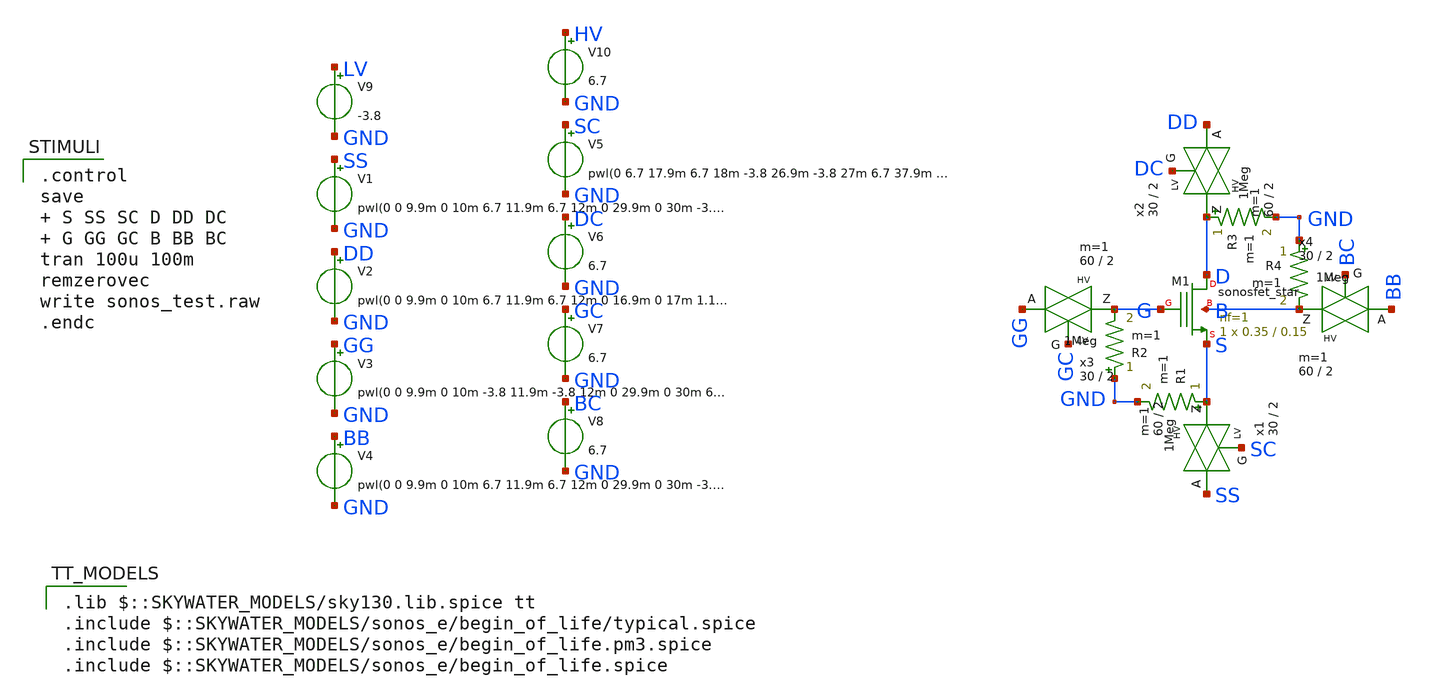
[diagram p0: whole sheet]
** sch_path: sonos_test.sch
* passgate_hv.sch:
* Copyright 2021 Stefan Frederik Schippers
* Licensed under the Apache License, Version 2.0 (the "License");
**.subckt sonos_test
XM1 D G S B sky130_fd_bs_flash__special_sonosfet_star L=0.15 W=0.35 ad=0.1015 as=0.1015 pd=1.28
+ ps=1.28 nrd=0.828571 nrs=0.828571 mult=1
V1 SS GND pwl(0 0 9.9m 0 10m 6.7 11.9m 6.7 12m 0 29.9m 0 30m -3.8 35.9m -3.8 36m 0 50m 0) r=0
V2 DD GND pwl(0 0 9.9m 0 10m 6.7 11.9m 6.7 12m 0 16.9m 0 17m 1.1 27.9m 1.1 28m 0 29.9m 0 30m -3.8
+ 35.9m -3.8 36m 0 36.9m 0 37m 1.1 47.9m 1.1 48m 0 50m 0) r=0
V3 GG GND pwl(0 0 9.9m 0 10m -3.8 11.9m -3.8 12m 0 29.9m 0 30m 6.7 35.9m 6.7 36m 0 50m 0) r=0
V4 BB GND pwl(0 0 9.9m 0 10m 6.7 11.9m 6.7 12m 0 29.9m 0 30m -3.8 35.9m -3.8 36m 0 50m 0) r=0
x1 S SS SC HV LV passgate_hv W_N=30 L_N=2 W_P=60 L_P=2 m=1
x2 D DD DC HV LV passgate_hv W_N=30 L_N=2 W_P=60 L_P=2 m=1
x3 G GG GC HV LV passgate_hv W_N=30 L_N=2 W_P=60 L_P=2 m=1
x4 B BB BC HV LV passgate_hv W_N=30 L_N=2 W_P=60 L_P=2 m=1
V5 SC GND pwl(0 6.7 17.9m 6.7 18m -3.8 26.9m -3.8 27m 6.7 37.9m 6.7 38m -3.8 46.9m -3.8 47m 6.7 50m
+ 6.7) r=0
V6 DC GND 6.7
V7 GC GND 6.7
V8 BC GND 6.7
V9 LV GND -3.8
V10 HV GND 6.7
R1 S GND 1Meg m=1
R2 GND G 1Meg m=1
R3 D GND 1Meg m=1
R4 GND B 1Meg m=1
**** begin user architecture code

.control
save  S SS SC D DD DC  G GG GC B BB BC
tran 100u 100m
remzerovec
write sonos_test.raw
.endc

 .lib $::SKYWATER_MODELS/sky130.lib.spice tt
.include $::SKYWATER_MODELS/sonos_e/begin_of_life/typical.spice
.include $::SKYWATER_MODELS/sonos_e/begin_of_life.pm3.spice
.include $::SKYWATER_MODELS/sonos_e/begin_of_life.spice
**** end user architecture code
**.ends

* expanding   symbol:  passgate_hv.sym # of pins=3
** sym_path: passgate_hv.sym
** sch_path: passgate_hv.sch
.subckt passgate_hv Z A G VCCBPIN VSSBPIN  W_N=30 L_N=2 W_P=60 L_P=2
*.iopin A
*.iopin Z
*.ipin G
XM2 A net1 Z VCCBPIN sky130_fd_pr__pfet_20v0 L=L_P W=W_P m=1
XM1 A G Z VSSBPIN sky130_fd_pr__nfet_20v0 L=L_N W=W_N m=1
XM3 net1 G VSSBPIN VSSBPIN sky130_fd_pr__nfet_20v0 L=L_N W=W_N m=1
XM4 net1 G VCCBPIN VCCBPIN sky130_fd_pr__pfet_20v0 L=L_P W=W_P m=1
.ends

.end
